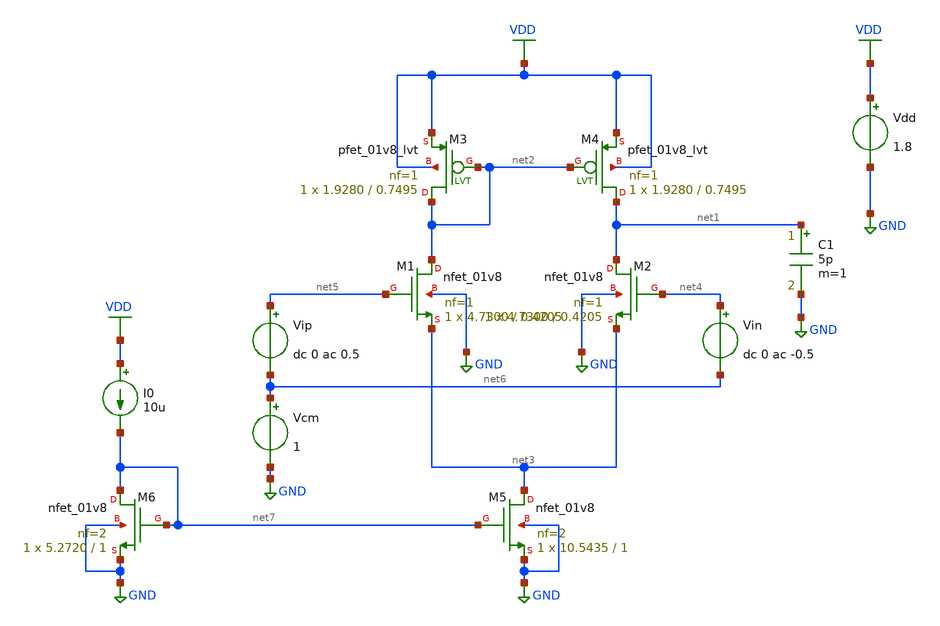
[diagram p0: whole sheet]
** sch_path: part1-basic-gain-gbw/cir/part1_OTA_basic_0.sch
**.subckt part1_OTA_basic_0
XM1 net2 net5 net3 GND sky130_fd_pr__nfet_01v8 L=0.4205 W=4.7300 nf=1 ad='int((1 + 1)/2) * 4.7300 / 1 * 0.29'
+ as='int((1 + 2)/2) * 4.7300 / 1 * 0.29' pd='2*int((1 + 1)/2) * (4.7300 / 1 + 0.29)' ps='2*int((1 + 2)/2) * (4.7300 / 1 + 0.29)'
+ nrd='0.29 / 4.7300 ' nrs='0.29 / 4.7300 ' sa=0 sb=0 sd=0 mult=1 m=1
XM5 net3 net7 GND GND sky130_fd_pr__nfet_01v8 L=1 W=10.5435 nf=2 ad='int((2 + 1)/2) * 10.5435 / 2 * 0.29'
+ as='int((2 + 2)/2) * 10.5435 / 2 * 0.29' pd='2*int((2 + 1)/2) * (10.5435 / 2 + 0.29)' ps='2*int((2 + 2)/2) * (10.5435 / 2 + 0.29)'
+ nrd='0.29 / 10.5435 ' nrs='0.29 / 10.5435 ' sa=0 sb=0 sd=0 mult=1 m=1
Vdd VDD GND 1.8
Vcm net6 GND 1
XM2 net1 net4 net3 GND sky130_fd_pr__nfet_01v8 L=0.4205 W=4.7300 nf=1 ad='int((1 + 1)/2) * 4.7300 / 1 * 0.29'
+ as='int((1 + 2)/2) * 4.7300 / 1 * 0.29' pd='2*int((1 + 1)/2) * (4.7300 / 1 + 0.29)' ps='2*int((1 + 2)/2) * (4.7300 / 1 + 0.29)'
+ nrd='0.29 / 4.7300 ' nrs='0.29 / 4.7300 ' sa=0 sb=0 sd=0 mult=1 m=1
Vip net5 net6 dc 0 ac 0.5
Vin net4 net6 dc 0 ac -0.5
C1 net1 GND 5p m=1
XM4 net1 net2 VDD VDD sky130_fd_pr__pfet_01v8_lvt L=0.7495 W=1.9280 nf=1 ad='int((1 + 1)/2) * 1.9280 / 1 * 0.29'
+ as='int((1 + 2)/2) * 1.9280 / 1 * 0.29' pd='2*int((1 + 1)/2) * (1.9280 / 1 + 0.29)' ps='2*int((1 + 2)/2) * (1.9280 / 1 + 0.29)'
+ nrd='0.29 / 1.9280 ' nrs='0.29 / 1.9280 ' sa=0 sb=0 sd=0 mult=1 m=1
XM3 net2 net2 VDD VDD sky130_fd_pr__pfet_01v8_lvt L=0.7495 W=1.9280 nf=1 ad='int((1 + 1)/2) * 1.9280 / 1 * 0.29'
+ as='int((1 + 2)/2) * 1.9280 / 1 * 0.29' pd='2*int((1 + 1)/2) * (1.9280 / 1 + 0.29)' ps='2*int((1 + 2)/2) * (1.9280 / 1 + 0.29)'
+ nrd='0.29 / 1.9280 ' nrs='0.29 / 1.9280 ' sa=0 sb=0 sd=0 mult=1 m=1
XM6 net7 net7 GND GND sky130_fd_pr__nfet_01v8 L=1 W=5.2720 nf=2 ad='int((2 + 1)/2) * 5.2720 / 2 * 0.29'
+ as='int((2 + 2)/2) * 5.2720 / 2 * 0.29' pd='2*int((2 + 1)/2) * (5.2720 / 2 + 0.29)' ps='2*int((2 + 2)/2) * (5.2720 / 2 + 0.29)'
+ nrd='0.29 / 5.2720 ' nrs='0.29 / 5.2720 ' sa=0 sb=0 sd=0 mult=1 m=1
I0 VDD net7 10u
**** begin user architecture code


.lib /foss/pdks/sky130A/libs.tech/ngspice/sky130.lib.spice tt


* - Print the operating points
.op

.control
	save @m.xm1.msky130_fd_pr__nfet_01v8[gm]
	save @m.xm1.msky130_fd_pr__nfet_01v8[id]
	save @m.xm1.msky130_fd_pr__nfet_01v8[gds]

	save @m.xm2.msky130_fd_pr__nfet_01v8[gm]
	save @m.xm2.msky130_fd_pr__nfet_01v8[id]
	save @m.xm2.msky130_fd_pr__nfet_01v8[gds]

	save @m.xm3.msky130_fd_pr__pfet_01v8_lvt[gm]
	save @m.xm3.msky130_fd_pr__pfet_01v8_lvt[id]
	save @m.xm3.msky130_fd_pr__pfet_01v8_lvt[gds]

	save @m.xm4.msky130_fd_pr__pfet_01v8_lvt[gm]
	save @m.xm4.msky130_fd_pr__pfet_01v8_lvt[id]
	save @m.xm4.msky130_fd_pr__pfet_01v8_lvt[gds]

	save @m.xm5.msky130_fd_pr__nfet_01v8[gm]
	save @m.xm5.msky130_fd_pr__nfet_01v8[id]
	save @m.xm5.msky130_fd_pr__nfet_01v8[gds]

	save @m.xm5.msky130_fd_pr__nfet_01v8[gm]
	save @m.xm5.msky130_fd_pr__nfet_01v8[id]
	save @m.xm5.msky130_fd_pr__nfet_01v8[gds]


	save all

	run

	show xm1.msky130_fd_pr__nfet_01v8
	show xm2.msky130_fd_pr__nfet_01v8
	show xm3.msky130_fd_pr__pfet_01v8_lvt
	show xm4.msky130_fd_pr__pfet_01v8_lvt
	show xm5.msky130_fd_pr__nfet_01v8
	show xm6.msky130_fd_pr__nfet_01v8
	show all


.endc




.lib /foss/pdks/sky130A/libs.tech/ngspice/sky130.lib.spice tt



.control

	save all

	ac dec 20 1 100e6

	meas ac dc_gain MAX vdb(net1) from=1 to=10
	let target_gain = dc_gain -3
	meas ac f_3db WHEN vdb(net1) = target_gain
	meas ac gbw WHEN vdb(net1) = 0

	let Av = vdb(net1)

	plot Av title 'DC Gain (Magnitude)'
	plot cph(net1)*180/pi title 'DC Gain (Phase)'

.endc




.lib /foss/pdks/sky130A/libs.tech/ngspice/sky130.lib.spice tt


* - Sweep Vcm and find the optimal operating point (gm, gds, id, biasing, etc)
.dc Vcm 0 1.8 0.1


.control
	save @m.xm1.msky130_fd_pr__nfet_01v8[gm]
	save @m.xm1.msky130_fd_pr__nfet_01v8[id]
	save @m.xm1.msky130_fd_pr__nfet_01v8[gds]

	save @m.xm2.msky130_fd_pr__nfet_01v8[gm]
	save @m.xm2.msky130_fd_pr__nfet_01v8[id]
	save @m.xm2.msky130_fd_pr__nfet_01v8[gds]

	save @m.xm3.msky130_fd_pr__pfet_01v8_lvt[gm]
	save @m.xm3.msky130_fd_pr__pfet_01v8_lvt[id]
	save @m.xm3.msky130_fd_pr__pfet_01v8_lvt[gds]

	save @m.xm4.msky130_fd_pr__pfet_01v8_lvt[gm]
	save @m.xm4.msky130_fd_pr__pfet_01v8_lvt[id]
	save @m.xm4.msky130_fd_pr__pfet_01v8_lvt[gds]

	save @m.xm5.msky130_fd_pr__nfet_01v8[gm]
	save @m.xm5.msky130_fd_pr__nfet_01v8[id]
	save @m.xm5.msky130_fd_pr__nfet_01v8[gds]

	save @m.xm5.msky130_fd_pr__nfet_01v8[gm]
	save @m.xm5.msky130_fd_pr__nfet_01v8[id]
	save @m.xm5.msky130_fd_pr__nfet_01v8[gds]

	save all

	run

	let gm_1_2 = @m.xm1.msky130_fd_pr__nfet_01v8[gm]
	let i5 = @m.xm5.msky130_fd_pr__nfet_01v8[id]

	plot gm_1_2 title 'VCM vs gm_12'
	plot i5 title 'VCM vs ISS'
	plot v(net2)-v(net3) title 'VCM vs Vds_12'
	plot v(vdd)-v(net2) title 'VCM vs Vds_34'
	plot v(net3) title 'VCM vs Vds_5'

.endc


**** end user architecture code
**.ends
.GLOBAL GND
.GLOBAL VDD
.end
